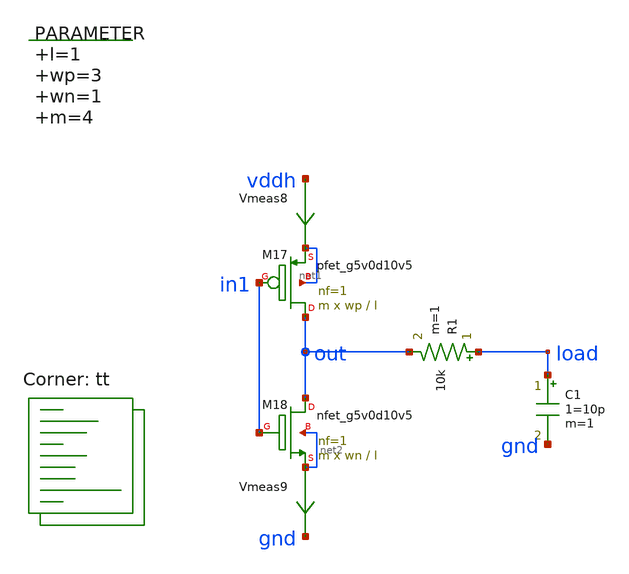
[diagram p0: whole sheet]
** sch_path: xschem/op_amp_class_AB_stage.sch
**.subckt op_amp_class_AB_stage
.param l=1 wp=3 wn=1 m=4
XM17 out in1 net1 net1 sky130_fd_pr__pfet_g5v0d10v5 L=l W=wp nf=1 ad='int((nf+1)/2) * W/nf * 0.29' as='int((nf+2)/2) * W/nf * 0.29'
+ pd='2*int((nf+1)/2) * (W/nf + 0.29)' ps='2*int((nf+2)/2) * (W/nf + 0.29)' nrd='0.29 / W' nrs='0.29 / W'
+ sa=0 sb=0 sd=0 mult=m m=m
XM18 out in1 net2 net2 sky130_fd_pr__nfet_g5v0d10v5 L=l W=wn nf=1 ad='int((nf+1)/2) * W/nf * 0.29' as='int((nf+2)/2) * W/nf * 0.29'
+ pd='2*int((nf+1)/2) * (W/nf + 0.29)' ps='2*int((nf+2)/2) * (W/nf + 0.29)' nrd='0.29 / W' nrs='0.29 / W'
+ sa=0 sb=0 sd=0 mult=m m=m
R1 load out 10k m=1
Vmeas8 vddh net1 0
.save i(vmeas8)
Vmeas9 net2 gnd 0
.save i(vmeas9)
C1 load gnd 1=10p m=1
**** begin user architecture code
.lib $::SKYWATER_MODELS/sky130.lib.spice tt



  .option wnflag=1
  .option safecurrents
  ********************Static Current Sources***************************
  Ivp vp gnd 5u
  Ivn vddh vn 5u
  Iip vddh ip 1u
  Iin in gnd 1u
  ********************Static Voltage Sources***************************
  Vddh vddh gnd dc 5.5

  vb1 vb1 gnd dc 3.37
  vb2 vb2 gnd dc 1.95
  ********************Dynamic Voltage Sources***************************
  *******Calculation**********
  .param base_f=100e3 base_t={1/base_f} base_th={base_t/2} base_d={base_th}
  .param d2_th ={base_th} d2_t={2*d2_th}
  .param d1_th ={4*d2_th} d1_t={d0_th}
  .param d0_th ={4*d1_th} d0_t={4*d0_th}

  .param d20_d ={0} d21_d={1*d2_th} d22_d={2*d2_th} d23_d={3*d2_th}
  .param d10_d ={0} d11_d={1*d1_th} d12_d={2*d1_th} d13_d={3*d1_th}
  .param d00_d ={0} d01_d={1*d0_th} d02_d={2*d0_th} d03_d={3*d0_th}
  *******Signals**********
  .param vhi=5.5
*  Vin1 b[0] gnd pulse(0 {vhi} {0} 1p 1p {10u} {20u})
*  Vin2 b[1] gnd pulse(0 {vhi} {0} 1p 1p {20u} {40u})
  vin1 in1 gnd sin({5.5/2} {5.5/2} 100k)
*  vin2 iny gnd sin({5.5/2} {-5.5/2} 100k)
  ********************Simulation Commands*****************************
  .control
     reset
     save all
     *dc vin 0 5.5 0.001
     *dc Iy 0 1u 0.001u
     dc vin1 0 5.5 0.01
*     tran 1n 50u
     write AB_stage-tb.raw
     set appendwrite
*    quit 0
  .endc



**** end user architecture code
**.ends
.end
